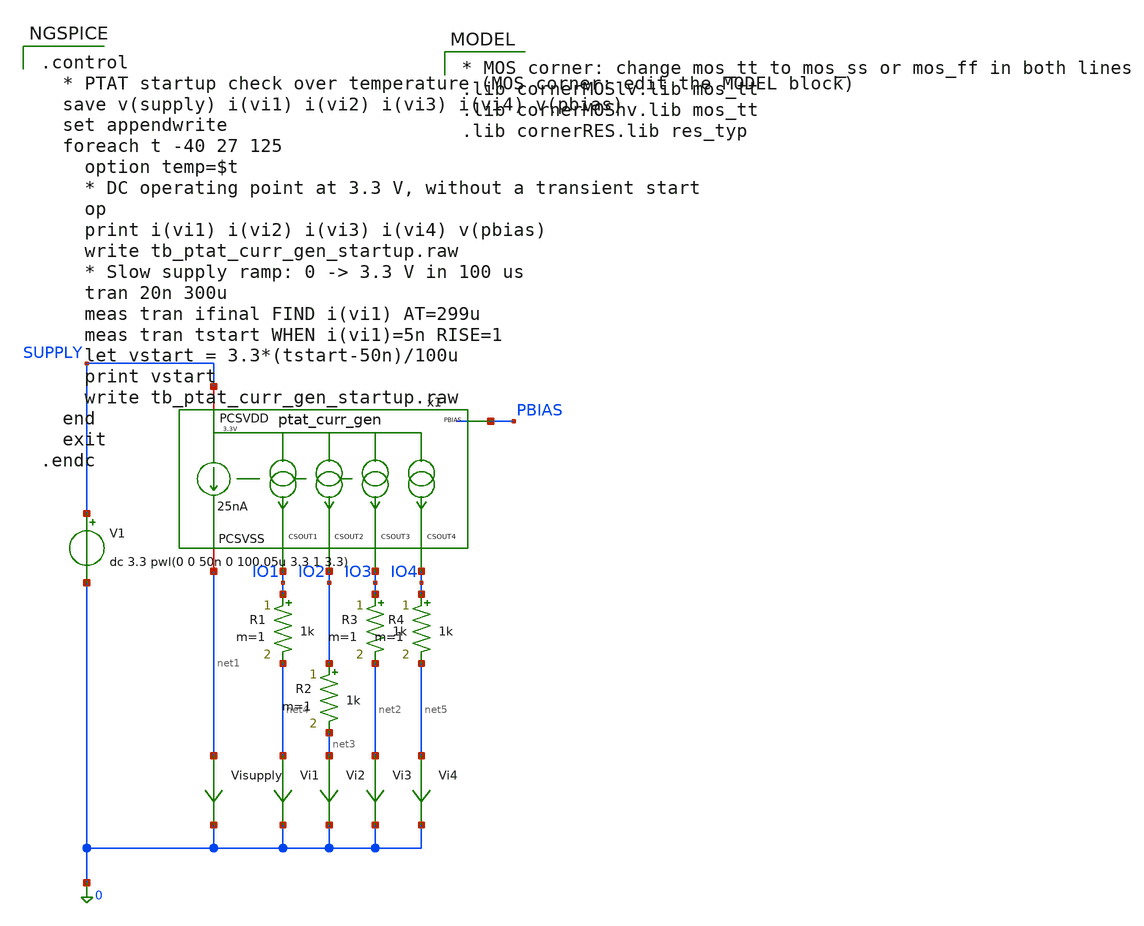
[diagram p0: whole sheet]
** sch_path: macros/heichips26_FAIf/macros/ptat_current_source/testbenches/xschem/tb_ptat_curr_gen_startup.sch
**.subckt tb_ptat_curr_gen_startup
V1 SUPPLY 0 dc 3.3 pwl(0 0 50n 0 100.05u 3.3 1 3.3)
R2 IO2 net3 1k m=1
R1 IO1 net4 1k m=1
R3 IO3 net2 1k m=1
Vi1 net4 0 0
.save i(vi1)
Vi2 net3 0 0
.save i(vi2)
Vi3 net2 0 0
.save i(vi3)
Vi4 net5 0 0
.save i(vi4)
R4 IO4 net5 1k m=1
Visupply net1 0 0
.save i(visupply)
x1 SUPPLY IO1 IO2 IO3 PBIAS net1 IO4 ptat_curr_gen
**** begin user architecture code

.control
  * PTAT startup check over temperature (MOS corner: edit the MODEL block)
  save v(supply) i(vi1) i(vi2) i(vi3) i(vi4) v(pbias)
  set appendwrite
  foreach t -40 27 125
    option temp=$t
    * DC operating point at 3.3 V, without a transient start
    op
    print i(vi1) i(vi2) i(vi3) i(vi4) v(pbias)
    write tb_ptat_curr_gen_startup.raw
    * Slow supply ramp: 0 -> 3.3 V in 100 us
    tran 20n 300u
    meas tran ifinal FIND i(vi1) AT=299u
    meas tran tstart WHEN i(vi1)=5n RISE=1
    let vstart = 3.3*(tstart-50n)/100u
    print vstart
    write tb_ptat_curr_gen_startup.raw
  end
  exit
.endc



* MOS corner: change mos_tt to mos_ss or mos_ff in both lines
.lib cornerMOSlv.lib mos_tt
.lib cornerMOShv.lib mos_tt
.lib cornerRES.lib res_typ


**** end user architecture code
**.ends

* expanding   symbol:  ptat_curr_gen.sym # of pins=7
** sym_path: macros/heichips26_FAIf/macros/ptat_current_source/schematic/xschem/ptat_curr_gen.sym
** sch_path: macros/heichips26_FAIf/macros/ptat_current_source/schematic/xschem/ptat_curr_gen.sch
.subckt ptat_curr_gen PCSVDD CSOUT1 CSOUT2 CSOUT3 PBIAS PCSVSS CSOUT4
*.iopin PCSVDD
*.iopin PCSVSS
*.opin CSOUT1
*.opin CSOUT2
*.opin CSOUT3
*.opin PBIAS
*.opin CSOUT4
XM1 net1 net1 PCSVSS PCSVSS sg13_hv_nmos w=2u l=2u ng=1 m=1 mm_ok=1
XM2 PBIAS net1 res_tap PCSVSS sg13_hv_nmos w=10u l=2u ng=1 m=1 mm_ok=1
XM3 net1 PBIAS PCSVDD PCSVDD sg13_hv_pmos w=0.4u l=1u ng=1 m=1 mm_ok=1
XM4 PBIAS PBIAS PCSVDD PCSVDD sg13_hv_pmos w=0.4u l=1u ng=1 m=1 mm_ok=1
XR1 res_tap PCSVSS PCSVSS rhigh w=0.5e-6 l=30e-6 m=1 b=21 mm_ok=1
XM5 CSOUT3 PBIAS PCSVDD PCSVDD sg13_hv_pmos w=0.4u l=1u ng=1 m=1 mm_ok=1
XM6 CSOUT2 PBIAS PCSVDD PCSVDD sg13_hv_pmos w=0.4u l=1u ng=1 m=1 mm_ok=1
XM7 CSOUT1 PBIAS PCSVDD PCSVDD sg13_hv_pmos w=0.4u l=1u ng=1 m=1 mm_ok=1
XMD1 PCSVSS PCSVSS PCSVSS PCSVSS sg13_hv_nmos w=10u l=2u ng=1 m=1 mm_ok=1
XMD2 PCSVSS PCSVSS PCSVSS PCSVSS sg13_hv_nmos w=10u l=2u ng=1 m=1 mm_ok=1
XMD3 PCSVSS PCSVSS PCSVSS PCSVSS sg13_hv_nmos w=5u l=2u ng=1 m=1 mm_ok=1
XMD4 PCSVSS PCSVSS PCSVSS PCSVSS sg13_hv_nmos w=5u l=2u ng=1 m=1 mm_ok=1
XMD5 PCSVSS PCSVSS PCSVSS PCSVSS sg13_hv_nmos w=5u l=2u ng=1 m=1 mm_ok=1
XMD6 PCSVSS PCSVSS PCSVSS PCSVSS sg13_hv_nmos w=5u l=2u ng=1 m=1 mm_ok=1
XMD7 PCSVSS PCSVSS PCSVSS PCSVSS sg13_hv_nmos w=5u l=2u ng=1 m=1 mm_ok=1
XMD8 PCSVSS PCSVSS PCSVSS PCSVSS sg13_hv_nmos w=5u l=2u ng=1 m=1 mm_ok=1
XMD9 PCSVSS PCSVSS PCSVSS PCSVSS sg13_hv_nmos w=2u l=2u ng=1 m=1 mm_ok=1
XMD10 PCSVSS PCSVSS PCSVSS PCSVSS sg13_hv_nmos w=2u l=2u ng=1 m=1 mm_ok=1
XMD11 PCSVSS PCSVSS PCSVSS PCSVSS sg13_hv_nmos w=1u l=2u ng=1 m=1 mm_ok=1
XMD12 PCSVSS PCSVSS PCSVSS PCSVSS sg13_hv_nmos w=1u l=2u ng=1 m=1 mm_ok=1
XMD13 PCSVSS PCSVSS PCSVSS PCSVSS sg13_hv_nmos w=1u l=2u ng=1 m=1 mm_ok=1
XMD14 PCSVSS PCSVSS PCSVSS PCSVSS sg13_hv_nmos w=1u l=2u ng=1 m=1 mm_ok=1
XMD15 PCSVSS PCSVSS PCSVSS PCSVSS sg13_hv_nmos w=1u l=2u ng=1 m=1 mm_ok=1
XMD16 PCSVSS PCSVSS PCSVSS PCSVSS sg13_hv_nmos w=1u l=2u ng=1 m=1 mm_ok=1
XMD17 PCSVDD PCSVDD PCSVDD PCSVDD sg13_hv_pmos w=0.4u l=1u ng=1 m=1 mm_ok=1
XMD24 PCSVDD PCSVDD PCSVDD PCSVDD sg13_hv_pmos w=0.4u l=1u ng=1 m=1 mm_ok=1
XMD31 PCSVDD PCSVDD PCSVDD PCSVDD sg13_hv_pmos w=0.4u l=1u ng=1 m=1 mm_ok=1
XMD18 PCSVDD PCSVDD PCSVDD PCSVDD sg13_hv_pmos w=0.4u l=1u ng=1 m=1 mm_ok=1
XMD19 PCSVDD PCSVDD PCSVDD PCSVDD sg13_hv_pmos w=0.4u l=1u ng=1 m=1 mm_ok=1
XMD20 PCSVDD PCSVDD PCSVDD PCSVDD sg13_hv_pmos w=0.4u l=1u ng=1 m=1 mm_ok=1
XMD21 PCSVDD PCSVDD PCSVDD PCSVDD sg13_hv_pmos w=0.4u l=1u ng=1 m=1 mm_ok=1
XMD22 PCSVDD PCSVDD PCSVDD PCSVDD sg13_hv_pmos w=0.4u l=1u ng=1 m=1 mm_ok=1
XMD23 PCSVDD PCSVDD PCSVDD PCSVDD sg13_hv_pmos w=0.4u l=1u ng=1 m=1 mm_ok=1
XMD25 PCSVDD PCSVDD PCSVDD PCSVDD sg13_hv_pmos w=0.4u l=1u ng=1 m=1 mm_ok=1
XMD26 PCSVDD PCSVDD PCSVDD PCSVDD sg13_hv_pmos w=0.4u l=1u ng=1 m=1 mm_ok=1
XMD27 PCSVDD PCSVDD PCSVDD PCSVDD sg13_hv_pmos w=0.4u l=1u ng=1 m=1 mm_ok=1
XMD28 PCSVDD PCSVDD PCSVDD PCSVDD sg13_hv_pmos w=0.4u l=1u ng=1 m=1 mm_ok=1
XMD29 PCSVDD PCSVDD PCSVDD PCSVDD sg13_hv_pmos w=0.4u l=1u ng=1 m=1 mm_ok=1
XMD30 PCSVDD PCSVDD PCSVDD PCSVDD sg13_hv_pmos w=0.4u l=1u ng=1 m=1 mm_ok=1
XMD32 PCSVDD PCSVDD PCSVDD PCSVDD sg13_hv_pmos w=0.4u l=1u ng=1 m=1 mm_ok=1
XMD33 PCSVDD PCSVDD PCSVDD PCSVDD sg13_hv_pmos w=0.4u l=1u ng=1 m=1 mm_ok=1
XMD34 PCSVDD PCSVDD PCSVDD PCSVDD sg13_hv_pmos w=0.4u l=1u ng=1 m=1 mm_ok=1
XMD35 PCSVDD PCSVDD PCSVDD PCSVDD sg13_hv_pmos w=0.4u l=1u ng=1 m=1 mm_ok=1
XMD36 PCSVDD PCSVDD PCSVDD PCSVDD sg13_hv_pmos w=0.4u l=1u ng=1 m=1 mm_ok=1
XMS1 CSSTARTUP net2 PCSVDD PCSVDD sg13_hv_pmos w=0.4u l=1u ng=1 m=1 mm_ok=1
XMS3 PCSVSS CSSTARTUP net2 PCSVDD sg13_hv_pmos w=0.4u l=1u ng=1 m=1 mm_ok=1
XMSS5 wcs4 wcs4 CSSTARTUP CSSTARTUP sg13_hv_pmos w=0.3u l=0.4u ng=1 m=1 mm_ok=1
XM8 CSOUT4 PBIAS PCSVDD PCSVDD sg13_hv_pmos w=0.4u l=1u ng=1 m=1 mm_ok=1
XMSS4 wcs3 wcs3 wcs4 wcs4 sg13_hv_pmos w=0.3u l=0.4u ng=1 m=1 mm_ok=1
XMSS3 wcs2 wcs2 wcs3 wcs3 sg13_hv_pmos w=0.3u l=0.4u ng=1 m=1 mm_ok=1
XMSS2 wcs1 wcs1 wcs2 wcs2 sg13_hv_pmos w=0.3u l=0.4u ng=1 m=1 mm_ok=1
XMSS1 PCSVSS PCSVSS wcs1 wcs1 sg13_hv_pmos w=0.3u l=0.4u ng=1 m=1 mm_ok=1
.ends

.end
